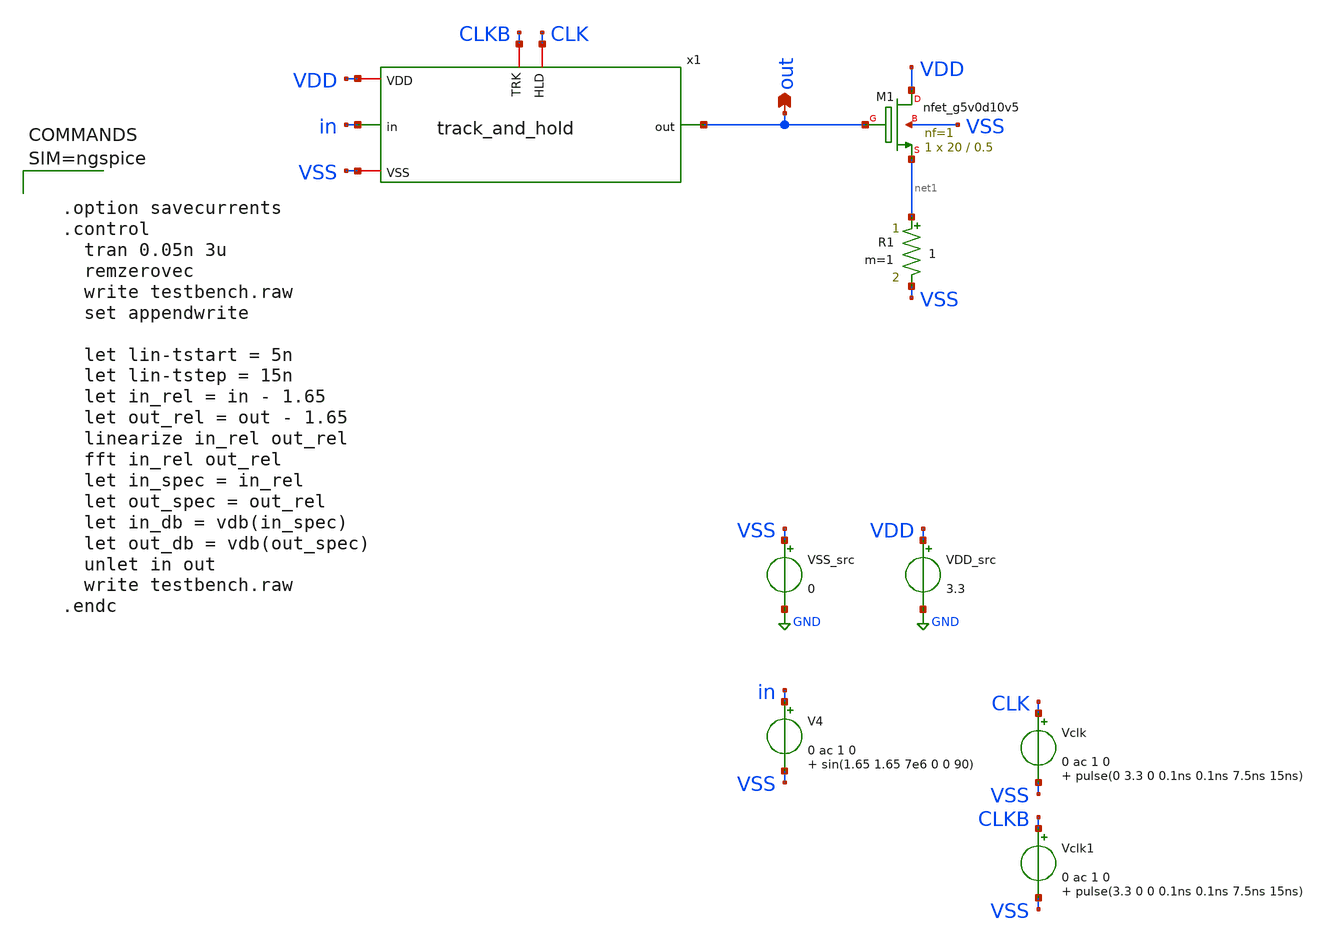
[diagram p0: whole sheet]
** sch_path: xschem/testbench.sch
**.subckt testbench out
*.opin out
VDD_src VDD GND 3.3
VSS_src VSS GND 0
V4 in VSS 0 ac 1 0 sin(1.65 1.65 7e6 0 0 90)
XM1 VDD out net1 VSS sky130_fd_pr__nfet_g5v0d10v5 L=0.5 W=20 nf=1 ad='int((nf+1)/2) * W/nf * 0.29' as='int((nf+2)/2) * W/nf * 0.29'
+ pd='2*int((nf+1)/2) * (W/nf + 0.29)' ps='2*int((nf+2)/2) * (W/nf + 0.29)' nrd='0.29 / W' nrs='0.29 / W'
+ sa=0 sb=0 sd=0 mult=1 m=1
R1 net1 VSS 1 m=1
Vclk CLK VSS 0 ac 1 0 pulse(0 3.3 0 0.1ns 0.1ns 7.5ns 15ns)
Vclk1 CLKB VSS 0 ac 1 0 pulse(3.3 0 0 0.1ns 0.1ns 7.5ns 15ns)
x1 CLK CLKB VDD VSS out in track_and_hold
**** begin user architecture code

** opencircuitdesign pdks install
.lib $::SKYWATER_MODELS/sky130.lib.spice tt





  .option savecurrents
  .control
    tran 0.05n 3u
    remzerovec
    write testbench.raw
    set appendwrite

    let lin-tstart = 5n
    let lin-tstep = 15n
    let in_rel = in - 1.65
    let out_rel = out - 1.65
    linearize in_rel out_rel
    fft in_rel out_rel
    let in_spec = in_rel
    let out_spec = out_rel
    let in_db = vdb(in_spec)
    let out_db = vdb(out_spec)
    unlet in out
    write testbench.raw
  .endc



**** end user architecture code
**.ends

* expanding   symbol:  track_and_hold.sym # of pins=6
** sym_path: xschem/track_and_hold.sym
** sch_path: xschem/track_and_hold.sch
.subckt track_and_hold HLD TRK VDD VSS out in
*.iopin VSS
*.iopin VDD
*.ipin in
*.opin out
*.iopin TRK
*.iopin HLD
XC1 out VSS sky130_fd_pr__cap_mim_m3_1 W=10 L=10 MF=1 m=1
V1 net2 in 3.3
XM1 out net1 in VSS sky130_fd_pr__nfet_g5v0d10v5 L=0.5 W=1 nf=1 ad='int((nf+1)/2) * W/nf * 0.29' as='int((nf+2)/2) * W/nf * 0.29'
+ pd='2*int((nf+1)/2) * (W/nf + 0.29)' ps='2*int((nf+2)/2) * (W/nf + 0.29)' nrd='0.29 / W' nrs='0.29 / W'
+ sa=0 sb=0 sd=0 mult=1 m=1
R1 VDD VSS 1G m=1
S2 net1 net2 TRK VSS SWITCH1
S4 net1 VSS HLD VSS SWITCH1
**** begin user architecture code



.model switch1 sw vt=1.65 vh=0 ron=1 roff=1G



**** end user architecture code
V2 in net3 3.3
S2p net4 net3 TRK VSS SWITCH1
S4p net4 VDD HLD VSS SWITCH1
XM2 out net4 in VDD sky130_fd_pr__pfet_g5v0d10v5 L=0.5 W=1.36 nf=1 ad='int((nf+1)/2) * W/nf * 0.29' as='int((nf+2)/2) * W/nf * 0.29'
+ pd='2*int((nf+1)/2) * (W/nf + 0.29)' ps='2*int((nf+2)/2) * (W/nf + 0.29)' nrd='0.29 / W' nrs='0.29 / W'
+ sa=0 sb=0 sd=0 mult=1 m=1
.ends

.GLOBAL GND
.end
